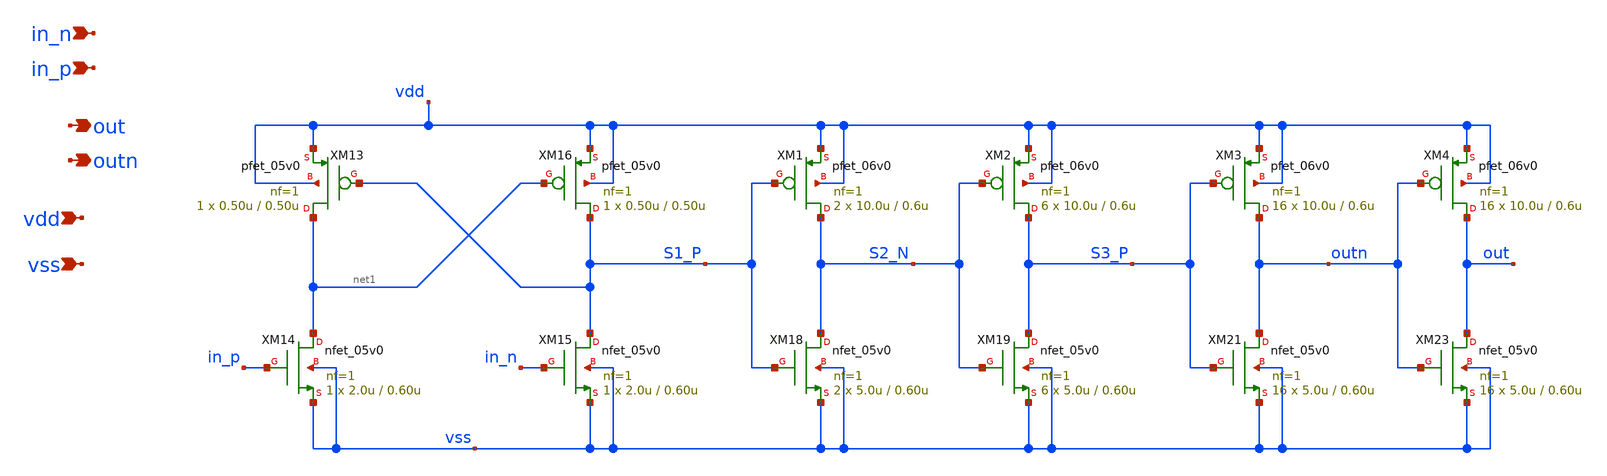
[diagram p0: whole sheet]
** sch_path: xschem/gate_drive_med.sch
**.subckt gate_drive_med in_n in_p vdd vss out outn
*.ipin in_n
*.ipin in_p
*.ipin vdd
*.ipin vss
*.opin out
*.opin outn
XM13 net1 S1_P vdd vdd pfet_05v0 L=0.50u W=0.50u nf=1 ad='int((nf+1)/2) * W/nf * 0.18u' as='int((nf+2)/2) * W/nf * 0.18u'
+ pd='2*int((nf+1)/2) * (W/nf + 0.18u)' ps='2*int((nf+2)/2) * (W/nf + 0.18u)' nrd='0.18u / W' nrs='0.18u / W'
+ sa=0 sb=0 sd=0 m=1 par=1
XM14 net1 in_p vss vss nfet_05v0 L=0.60u W=2.0u nf=1 ad='int((nf+1)/2) * W/nf * 0.18u' as='int((nf+2)/2) * W/nf * 0.18u'
+ pd='2*int((nf+1)/2) * (W/nf + 0.18u)' ps='2*int((nf+2)/2) * (W/nf + 0.18u)' nrd='0.18u / W' nrs='0.18u / W'
+ sa=0 sb=0 sd=0 m=1
XM15 S1_P in_n vss vss nfet_05v0 L=0.60u W=2.0u nf=1 ad='int((nf+1)/2) * W/nf * 0.18u' as='int((nf+2)/2) * W/nf * 0.18u'
+ pd='2*int((nf+1)/2) * (W/nf + 0.18u)' ps='2*int((nf+2)/2) * (W/nf + 0.18u)' nrd='0.18u / W' nrs='0.18u / W'
+ sa=0 sb=0 sd=0 m=1
XM16 S1_P net1 vdd vdd pfet_05v0 L=0.50u W=0.50u nf=1 ad='int((nf+1)/2) * W/nf * 0.18u' as='int((nf+2)/2) * W/nf * 0.18u'
+ pd='2*int((nf+1)/2) * (W/nf + 0.18u)' ps='2*int((nf+2)/2) * (W/nf + 0.18u)' nrd='0.18u / W' nrs='0.18u / W'
+ sa=0 sb=0 sd=0 m=1 par=1
XM18 S2_N S1_P vss vss nfet_05v0 L=0.60u W=5.0u nf=1 ad='int((nf+1)/2) * W/nf * 0.18u' as='int((nf+2)/2) * W/nf * 0.18u'
+ pd='2*int((nf+1)/2) * (W/nf + 0.18u)' ps='2*int((nf+2)/2) * (W/nf + 0.18u)' nrd='0.18u / W' nrs='0.18u / W'
+ sa=0 sb=0 sd=0 m=2
XM19 S3_P S2_N vss vss nfet_05v0 L=0.60u W=5.0u nf=1 ad='int((nf+1)/2) * W/nf * 0.18u' as='int((nf+2)/2) * W/nf * 0.18u'
+ pd='2*int((nf+1)/2) * (W/nf + 0.18u)' ps='2*int((nf+2)/2) * (W/nf + 0.18u)' nrd='0.18u / W' nrs='0.18u / W'
+ sa=0 sb=0 sd=0 m=6
XM21 outn S3_P vss vss nfet_05v0 L=0.60u W=5.0u nf=1 ad='int((nf+1)/2) * W/nf * 0.18u' as='int((nf+2)/2) * W/nf * 0.18u'
+ pd='2*int((nf+1)/2) * (W/nf + 0.18u)' ps='2*int((nf+2)/2) * (W/nf + 0.18u)' nrd='0.18u / W' nrs='0.18u / W'
+ sa=0 sb=0 sd=0 m=16
XM23 out outn vss vss nfet_05v0 L=0.60u W=5.0u nf=1 ad='int((nf+1)/2) * W/nf * 0.18u' as='int((nf+2)/2) * W/nf * 0.18u'
+ pd='2*int((nf+1)/2) * (W/nf + 0.18u)' ps='2*int((nf+2)/2) * (W/nf + 0.18u)' nrd='0.18u / W' nrs='0.18u / W'
+ sa=0 sb=0 sd=0 m=16
XM1 S2_N S1_P vdd vdd pfet_06v0 L=0.6u W=10.0u nf=1 ad='int((nf+1)/2) * W/nf * 0.18u' as='int((nf+2)/2) * W/nf * 0.18u'
+ pd='2*int((nf+1)/2) * (W/nf + 0.18u)' ps='2*int((nf+2)/2) * (W/nf + 0.18u)' nrd='0.18u / W' nrs='0.18u / W'
+ sa=0 sb=0 sd=0 m=2
XM2 S3_P S2_N vdd vdd pfet_06v0 L=0.6u W=10.0u nf=1 ad='int((nf+1)/2) * W/nf * 0.18u' as='int((nf+2)/2) * W/nf * 0.18u'
+ pd='2*int((nf+1)/2) * (W/nf + 0.18u)' ps='2*int((nf+2)/2) * (W/nf + 0.18u)' nrd='0.18u / W' nrs='0.18u / W'
+ sa=0 sb=0 sd=0 m=6
XM3 outn S3_P vdd vdd pfet_06v0 L=0.6u W=10.0u nf=1 ad='int((nf+1)/2) * W/nf * 0.18u' as='int((nf+2)/2) * W/nf * 0.18u'
+ pd='2*int((nf+1)/2) * (W/nf + 0.18u)' ps='2*int((nf+2)/2) * (W/nf + 0.18u)' nrd='0.18u / W' nrs='0.18u / W'
+ sa=0 sb=0 sd=0 m=16
XM4 out outn vdd vdd pfet_06v0 L=0.6u W=10.0u nf=1 ad='int((nf+1)/2) * W/nf * 0.18u' as='int((nf+2)/2) * W/nf * 0.18u'
+ pd='2*int((nf+1)/2) * (W/nf + 0.18u)' ps='2*int((nf+2)/2) * (W/nf + 0.18u)' nrd='0.18u / W' nrs='0.18u / W'
+ sa=0 sb=0 sd=0 m=16
**.ends
.end
